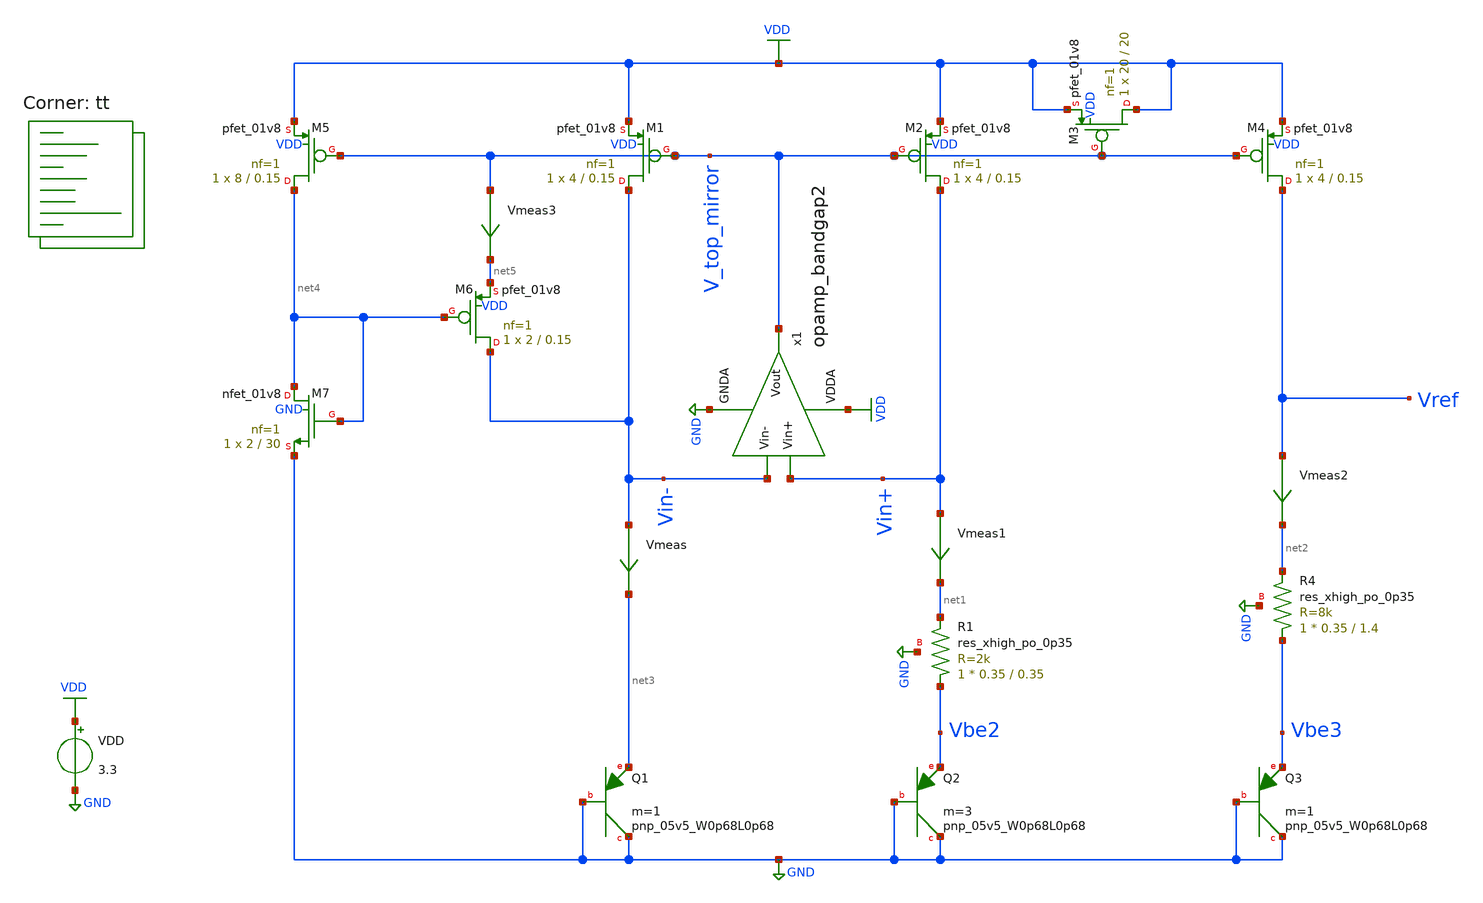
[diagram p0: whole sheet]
** sch_path: projects/pll/bandgapref/xschem_ngspice/mos_bandgap_baker3.sch
**.subckt mos_bandgap_baker3
XM1 Vin- V_top_mirror VDD VDD sky130_fd_pr__pfet_01v8 L=0.15 W=4 nf=1 ad='int((nf+1)/2) * W/nf * 0.29'
+ as='int((nf+2)/2) * W/nf * 0.29' pd='2*int((nf+1)/2) * (W/nf + 0.29)' ps='2*int((nf+2)/2) * (W/nf + 0.29)'
+ nrd='0.29 / W' nrs='0.29 / W' sa=0 sb=0 sd=0 mult=1 m=1
XM2 Vin+ V_top_mirror VDD VDD sky130_fd_pr__pfet_01v8 L=0.15 W=4 nf=1 ad='int((nf+1)/2) * W/nf * 0.29'
+ as='int((nf+2)/2) * W/nf * 0.29' pd='2*int((nf+1)/2) * (W/nf + 0.29)' ps='2*int((nf+2)/2) * (W/nf + 0.29)'
+ nrd='0.29 / W' nrs='0.29 / W' sa=0 sb=0 sd=0 mult=1 m=1
VDD VDD GND 3.3
Vmeas Vin- net3 0
.save i(vmeas)
Vmeas1 Vin+ net1 0
.save i(vmeas1)
XR1 Vbe2 net1 GND sky130_fd_pr__res_xhigh_po_0p35 L=0.35 mult=1 m=1
x1 VDD V_top_mirror Vin- Vin+ GND opamp_bandgap2
XQ1 GND GND net3 sky130_fd_pr__pnp_05v5_W0p68L0p68 m=1
XQ2 GND GND Vbe2 sky130_fd_pr__pnp_05v5_W0p68L0p68 m=3
XM4 Vref V_top_mirror VDD VDD sky130_fd_pr__pfet_01v8 L=0.15 W=4 nf=1 ad='int((nf+1)/2) * W/nf * 0.29'
+ as='int((nf+2)/2) * W/nf * 0.29' pd='2*int((nf+1)/2) * (W/nf + 0.29)' ps='2*int((nf+2)/2) * (W/nf + 0.29)'
+ nrd='0.29 / W' nrs='0.29 / W' sa=0 sb=0 sd=0 mult=1 m=1
XR4 Vbe3 net2 GND sky130_fd_pr__res_xhigh_po_0p35 L=1.4 mult=1 m=1
XQ3 GND GND Vbe3 sky130_fd_pr__pnp_05v5_W0p68L0p68 m=1
Vmeas2 Vref net2 0
.save i(vmeas2)
XM7 net4 net4 GND GND sky130_fd_pr__nfet_01v8 L=30 W=2 nf=1 ad='int((nf+1)/2) * W/nf * 0.29' as='int((nf+2)/2) * W/nf * 0.29'
+ pd='2*int((nf+1)/2) * (W/nf + 0.29)' ps='2*int((nf+2)/2) * (W/nf + 0.29)' nrd='0.29 / W' nrs='0.29 / W'
+ sa=0 sb=0 sd=0 mult=1 m=1
XM6 Vin- net4 net5 VDD sky130_fd_pr__pfet_01v8 L=0.15 W=2 nf=1 ad='int((nf+1)/2) * W/nf * 0.29' as='int((nf+2)/2) * W/nf * 0.29'
+ pd='2*int((nf+1)/2) * (W/nf + 0.29)' ps='2*int((nf+2)/2) * (W/nf + 0.29)' nrd='0.29 / W' nrs='0.29 / W'
+ sa=0 sb=0 sd=0 mult=1 m=1
XM5 net4 V_top_mirror VDD VDD sky130_fd_pr__pfet_01v8 L=0.15 W=8 nf=1 ad='int((nf+1)/2) * W/nf * 0.29'
+ as='int((nf+2)/2) * W/nf * 0.29' pd='2*int((nf+1)/2) * (W/nf + 0.29)' ps='2*int((nf+2)/2) * (W/nf + 0.29)'
+ nrd='0.29 / W' nrs='0.29 / W' sa=0 sb=0 sd=0 mult=1 m=1
XM3 VDD V_top_mirror VDD VDD sky130_fd_pr__pfet_01v8 L=20 W=20 nf=1 ad='int((nf+1)/2) * W/nf * 0.29'
+ as='int((nf+2)/2) * W/nf * 0.29' pd='2*int((nf+1)/2) * (W/nf + 0.29)' ps='2*int((nf+2)/2) * (W/nf + 0.29)'
+ nrd='0.29 / W' nrs='0.29 / W' sa=0 sb=0 sd=0 mult=1 m=1
Vmeas3 V_top_mirror net5 0
.save i(vmeas3)
**** begin user architecture code
.lib $::SKYWATER_MODELS/sky130.lib.spice tt



.option method=gear
.option wnflag=1
.option savecurrents

.save @m.xm1.msky130_fd_pr__pfet_01v8[gm] @m.xm2.msky130_fd_pr__pfet_01v8[gm] @m.xm3.msky130_fd_pr__pfet_01v8[gm] @m.xm4.msky130_fd_pr__pfet_01v8[gm] @m.xm5.msky130_fd_pr__pfet_01v8[gm] @m.xm6.msky130_fd_pr__pfet_01v8[gm] @m.xm7.msky130_fd_pr__nfet_01v8[gm]


.control
save all
op
dc VDD 0 3.3 0.1 temp -40 120 1
* tran 5ns 50us
remzerovec
write mos_bandgap_baker3.raw
.endc




**** end user architecture code
**.ends

* expanding   symbol:
*+  /foss/designs/my_design/projects/pll/bandgapref/xschem_ngspice/opamp_bandgap2.sym # of pins=5
** sym_path: projects/bandgapref/xschem_ngspice/old_files/opamp_bandgap2.sym
** sch_path: projects/bandgapref/xschem_ngspice/old_files/opamp_bandgap2.sch
.subckt opamp_bandgap2 VDDA Vout Vin- Vin+ GNDA
*.ipin Vin+
*.opin Vout
*.ipin Vin-
*.ipin GNDA
*.ipin VDDA
XM2 net2 Vin- net1 GNDA sky130_fd_pr__nfet_01v8 L=0.6 W=2 nf=2 ad='int((nf+1)/2) * W/nf * 0.29' as='int((nf+2)/2) * W/nf * 0.29'
+ pd='2*int((nf+1)/2) * (W/nf + 0.29)' ps='2*int((nf+2)/2) * (W/nf + 0.29)' nrd='0.29 / W' nrs='0.29 / W'
+ sa=0 sb=0 sd=0 mult=1 m=1
XM3 Vout Vin+ net1 GNDA sky130_fd_pr__nfet_01v8 L=0.6 W=2 nf=2 ad='int((nf+1)/2) * W/nf * 0.29' as='int((nf+2)/2) * W/nf * 0.29'
+ pd='2*int((nf+1)/2) * (W/nf + 0.29)' ps='2*int((nf+2)/2) * (W/nf + 0.29)' nrd='0.29 / W' nrs='0.29 / W'
+ sa=0 sb=0 sd=0 mult=1 m=1
XM1 net1 net1 GNDA GNDA sky130_fd_pr__nfet_01v8 L=0.6 W=4 nf=1 ad='int((nf+1)/2) * W/nf * 0.29' as='int((nf+2)/2) * W/nf * 0.29'
+ pd='2*int((nf+1)/2) * (W/nf + 0.29)' ps='2*int((nf+2)/2) * (W/nf + 0.29)' nrd='0.29 / W' nrs='0.29 / W'
+ sa=0 sb=0 sd=0 mult=1 m=1
XM4 Vout net2 VDDA VDDA sky130_fd_pr__pfet_01v8 L=0.6 W=4 nf=4 ad='int((nf+1)/2) * W/nf * 0.29' as='int((nf+2)/2) * W/nf * 0.29'
+ pd='2*int((nf+1)/2) * (W/nf + 0.29)' ps='2*int((nf+2)/2) * (W/nf + 0.29)' nrd='0.29 / W' nrs='0.29 / W'
+ sa=0 sb=0 sd=0 mult=1 m=1
XM5 net2 net2 VDDA VDDA sky130_fd_pr__pfet_01v8 L=0.6 W=4 nf=4 ad='int((nf+1)/2) * W/nf * 0.29' as='int((nf+2)/2) * W/nf * 0.29'
+ pd='2*int((nf+1)/2) * (W/nf + 0.29)' ps='2*int((nf+2)/2) * (W/nf + 0.29)' nrd='0.29 / W' nrs='0.29 / W'
+ sa=0 sb=0 sd=0 mult=1 m=1
.ends

.GLOBAL VDD
.GLOBAL GND
.end
